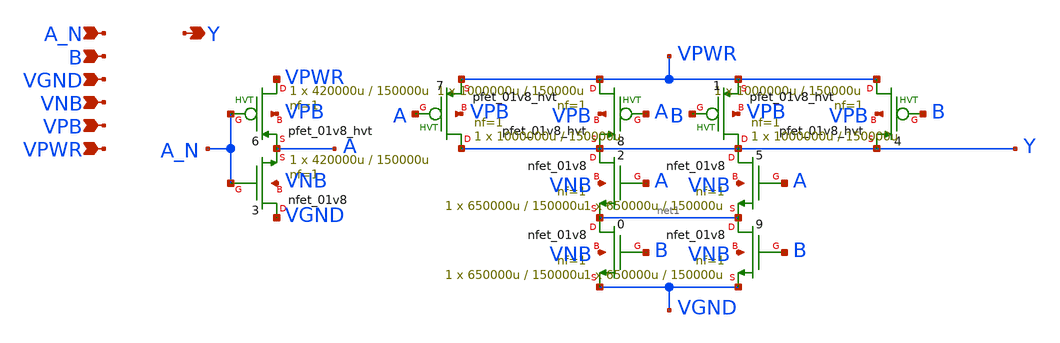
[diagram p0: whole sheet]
** sch_path: schematics/nand2b/sky130_fd_sc_hd__nand2b_2.sch
**.subckt sky130_fd_sc_hd__nand2b_2 A_N B VGND VNB VPB VPWR Y
*.ipin A_N
*.ipin B
*.ipin VGND
*.ipin VNB
*.ipin VPB
*.ipin VPWR
*.opin Y
X8 VPWR A Y VPB sky130_fd_pr__pfet_01v8_hvt L=150000u W=1000000u nf=1 ad='int((1 + 1)/2) * 1000000u / 1 * 0.29'
+ as='int((1 + 2)/2) * 1000000u / 1 * 0.29' pd='2*int((1 + 1)/2) * (1000000u / 1 + 0.29)' ps='2*int((1 + 2)/2) * (1000000u / 1 + 0.29)'
+ nrd='0.29 / 1000000u ' nrs='0.29 / 1000000u ' sa=0 sb=0 sd=0 mult=1 m=1
X7 Y A VPWR VPB sky130_fd_pr__pfet_01v8_hvt L=150000u W=1000000u nf=1 ad='int((1 + 1)/2) * 1000000u / 1 * 0.29'
+ as='int((1 + 2)/2) * 1000000u / 1 * 0.29' pd='2*int((1 + 1)/2) * (1000000u / 1 + 0.29)' ps='2*int((1 + 2)/2) * (1000000u / 1 + 0.29)'
+ nrd='0.29 / 1000000u ' nrs='0.29 / 1000000u ' sa=0 sb=0 sd=0 mult=1 m=1
X2 Y A net1 VNB sky130_fd_pr__nfet_01v8 L=150000u W=650000u nf=1 ad='int((1 + 1)/2) * 650000u / 1 * 0.29'
+ as='int((1 + 2)/2) * 650000u / 1 * 0.29' pd='2*int((1 + 1)/2) * (650000u / 1 + 0.29)' ps='2*int((1 + 2)/2) * (650000u / 1 + 0.29)'
+ nrd='0.29 / 650000u ' nrs='0.29 / 650000u ' sa=0 sb=0 sd=0 mult=1 m=1
X0 net1 B VGND VNB sky130_fd_pr__nfet_01v8 L=150000u W=650000u nf=1 ad='int((1 + 1)/2) * 650000u / 1 * 0.29'
+ as='int((1 + 2)/2) * 650000u / 1 * 0.29' pd='2*int((1 + 1)/2) * (650000u / 1 + 0.29)' ps='2*int((1 + 2)/2) * (650000u / 1 + 0.29)'
+ nrd='0.29 / 650000u ' nrs='0.29 / 650000u ' sa=0 sb=0 sd=0 mult=1 m=1
X3 VGND A_N A VNB sky130_fd_pr__nfet_01v8 L=150000u W=420000u nf=1 ad='int((1 + 1)/2) * 420000u / 1 * 0.29'
+ as='int((1 + 2)/2) * 420000u / 1 * 0.29' pd='2*int((1 + 1)/2) * (420000u / 1 + 0.29)' ps='2*int((1 + 2)/2) * (420000u / 1 + 0.29)'
+ nrd='0.29 / 420000u ' nrs='0.29 / 420000u ' sa=0 sb=0 sd=0 mult=1 m=1
X6 VPWR A_N A VPB sky130_fd_pr__pfet_01v8_hvt L=150000u W=420000u nf=1 ad='int((1 + 1)/2) * 420000u / 1 * 0.29'
+ as='int((1 + 2)/2) * 420000u / 1 * 0.29' pd='2*int((1 + 1)/2) * (420000u / 1 + 0.29)' ps='2*int((1 + 2)/2) * (420000u / 1 + 0.29)'
+ nrd='0.29 / 420000u ' nrs='0.29 / 420000u ' sa=0 sb=0 sd=0 mult=1 m=1
X5 Y A net1 VNB sky130_fd_pr__nfet_01v8 L=150000u W=650000u nf=1 ad='int((1 + 1)/2) * 650000u / 1 * 0.29'
+ as='int((1 + 2)/2) * 650000u / 1 * 0.29' pd='2*int((1 + 1)/2) * (650000u / 1 + 0.29)' ps='2*int((1 + 2)/2) * (650000u / 1 + 0.29)'
+ nrd='0.29 / 650000u ' nrs='0.29 / 650000u ' sa=0 sb=0 sd=0 mult=1 m=1
X9 net1 B VGND VNB sky130_fd_pr__nfet_01v8 L=150000u W=650000u nf=1 ad='int((1 + 1)/2) * 650000u / 1 * 0.29'
+ as='int((1 + 2)/2) * 650000u / 1 * 0.29' pd='2*int((1 + 1)/2) * (650000u / 1 + 0.29)' ps='2*int((1 + 2)/2) * (650000u / 1 + 0.29)'
+ nrd='0.29 / 650000u ' nrs='0.29 / 650000u ' sa=0 sb=0 sd=0 mult=1 m=1
X4 VPWR B Y VPB sky130_fd_pr__pfet_01v8_hvt L=150000u W=1000000u nf=1 ad='int((1 + 1)/2) * 1000000u / 1 * 0.29'
+ as='int((1 + 2)/2) * 1000000u / 1 * 0.29' pd='2*int((1 + 1)/2) * (1000000u / 1 + 0.29)' ps='2*int((1 + 2)/2) * (1000000u / 1 + 0.29)'
+ nrd='0.29 / 1000000u ' nrs='0.29 / 1000000u ' sa=0 sb=0 sd=0 mult=1 m=1
X1 Y B VPWR VPB sky130_fd_pr__pfet_01v8_hvt L=150000u W=1000000u nf=1 ad='int((1 + 1)/2) * 1000000u / 1 * 0.29'
+ as='int((1 + 2)/2) * 1000000u / 1 * 0.29' pd='2*int((1 + 1)/2) * (1000000u / 1 + 0.29)' ps='2*int((1 + 2)/2) * (1000000u / 1 + 0.29)'
+ nrd='0.29 / 1000000u ' nrs='0.29 / 1000000u ' sa=0 sb=0 sd=0 mult=1 m=1
**.ends
.end
